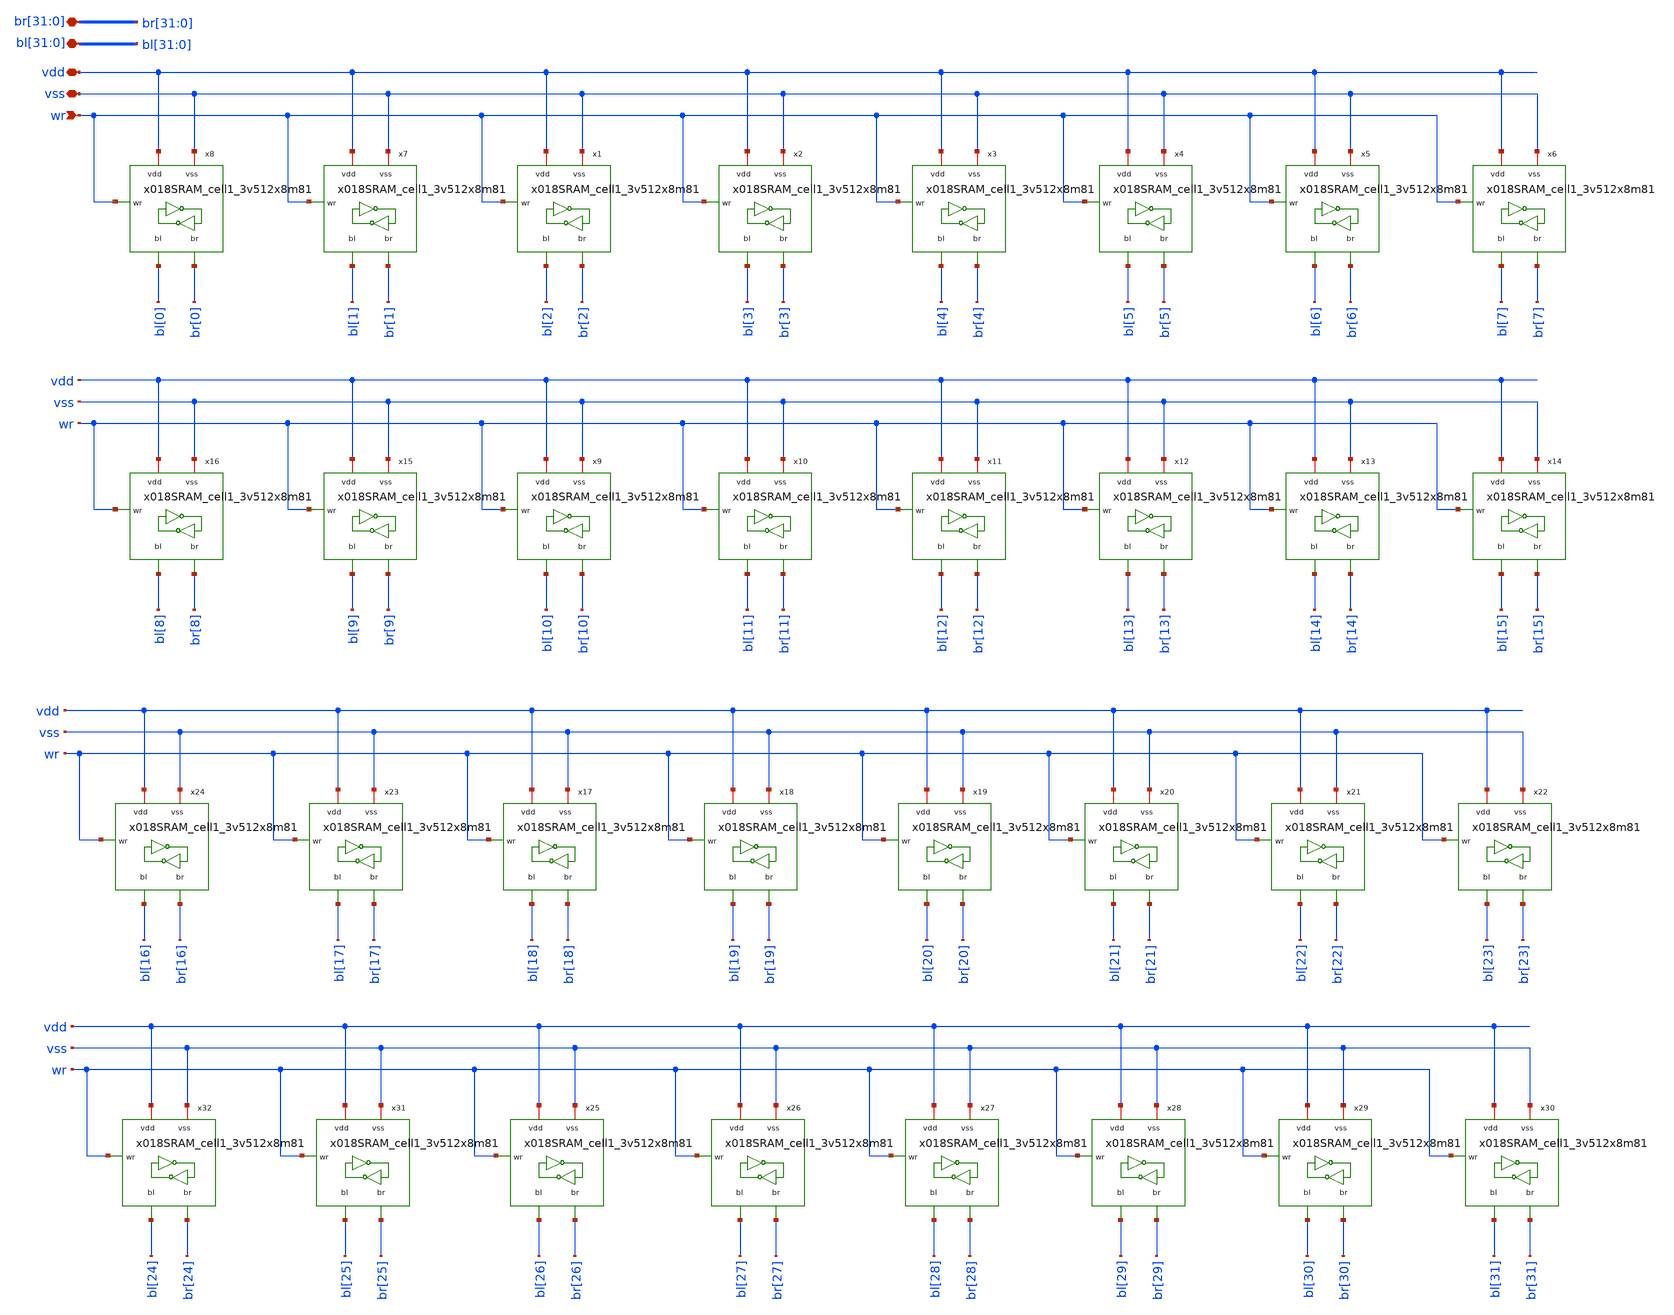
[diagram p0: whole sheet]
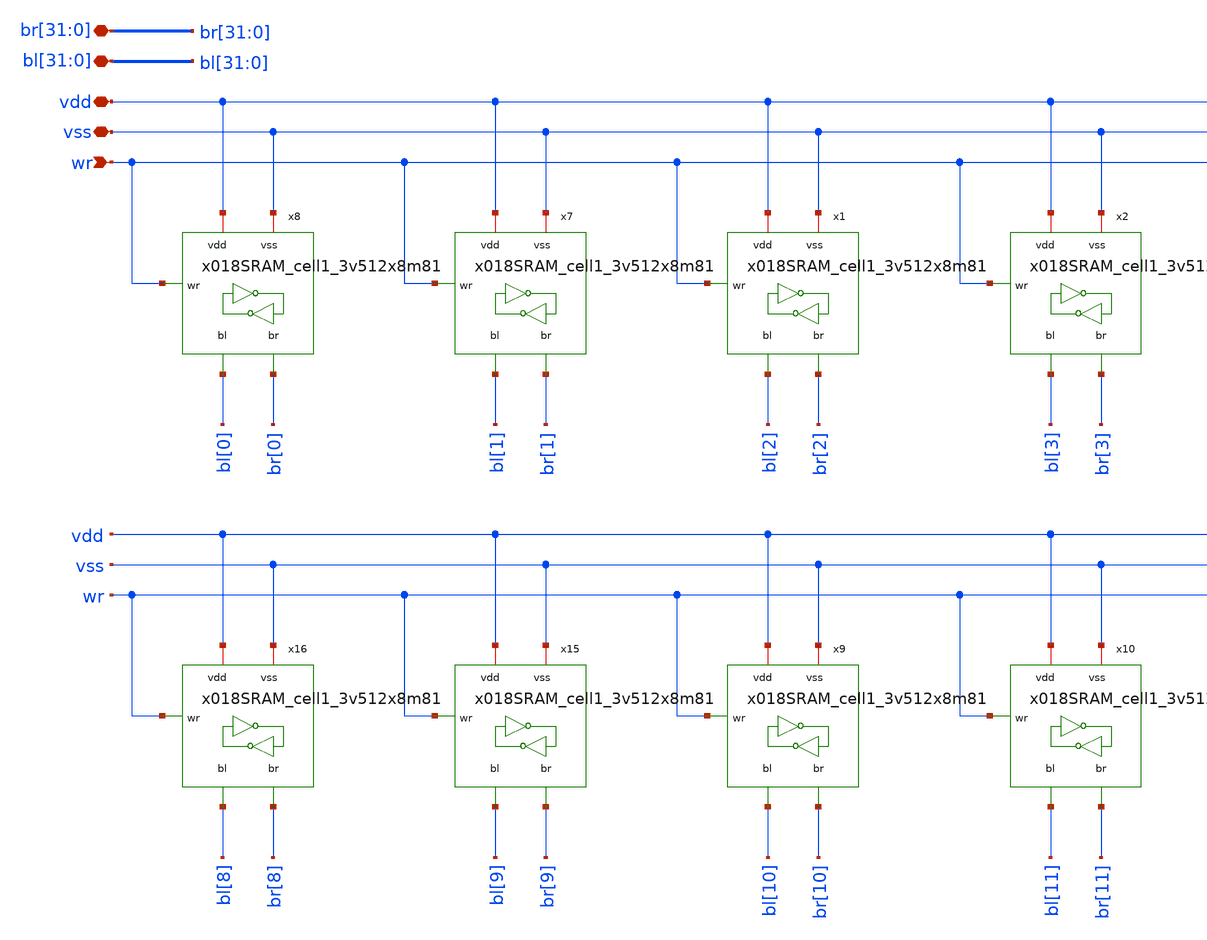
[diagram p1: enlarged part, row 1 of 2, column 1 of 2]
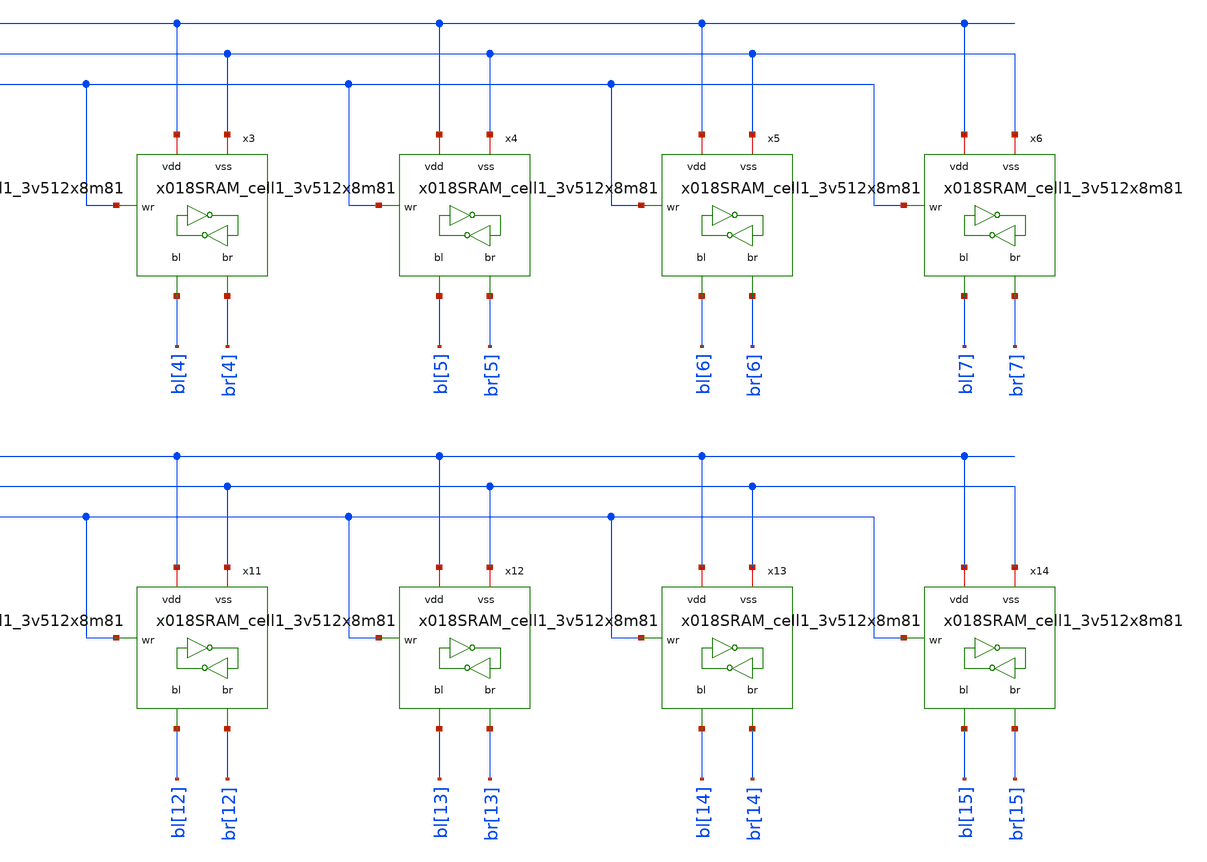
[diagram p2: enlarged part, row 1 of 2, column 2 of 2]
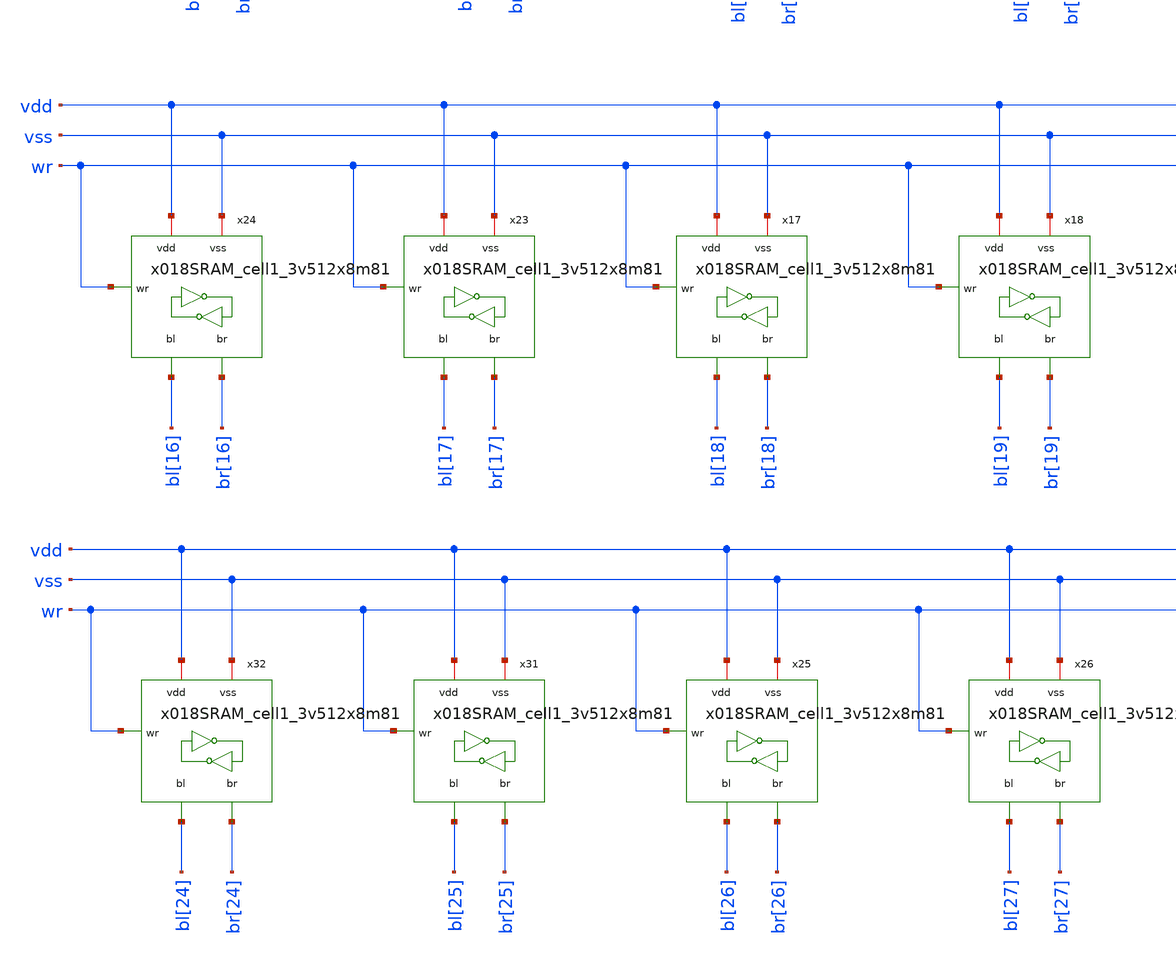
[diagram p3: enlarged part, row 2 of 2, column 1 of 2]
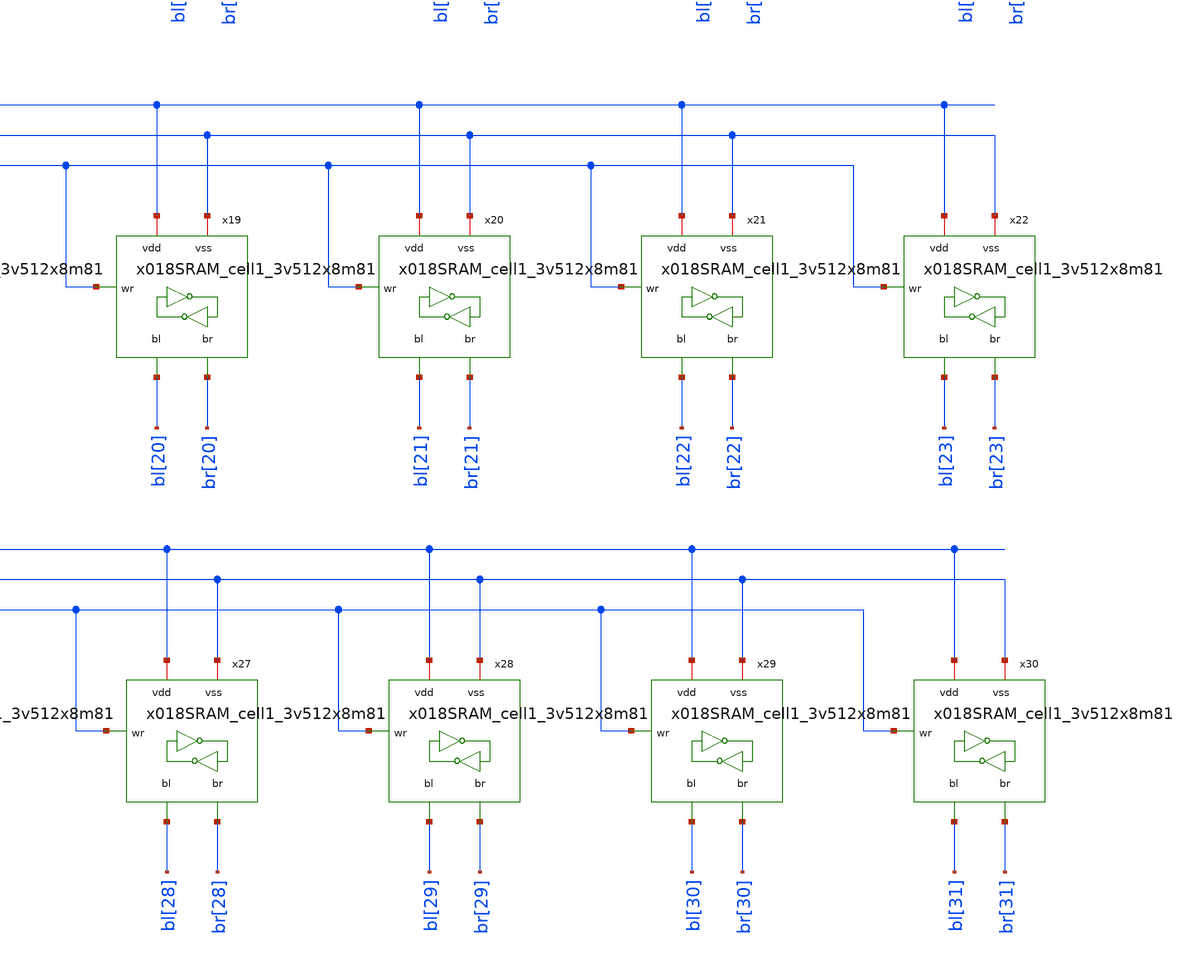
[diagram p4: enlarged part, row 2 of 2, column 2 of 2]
** sch_path: cells/gf180mcu_ocd_ip_sram__sram512x8m8wm1/xschem/Cell_array32x1_3v512x8m81.sch
**.subckt Cell_array32x1_3v512x8m81 vdd vss wr
*+ bl[31],bl[30],bl[29],bl[28],bl[27],bl[26],bl[25],bl[24],bl[23],bl[22],bl[21],bl[20],bl[19],bl[18],bl[17],bl[16],bl[15],bl[14],bl[13],bl[12],bl[11],bl[10],bl[9],bl[8],bl[7],bl[6],bl[5],bl[4],bl[3],bl[2],bl[1],bl[0]
*+ br[31],br[30],br[29],br[28],br[27],br[26],br[25],br[24],br[23],br[22],br[21],br[20],br[19],br[18],br[17],br[16],br[15],br[14],br[13],br[12],br[11],br[10],br[9],br[8],br[7],br[6],br[5],br[4],br[3],br[2],br[1],br[0]
*.iopin vdd
*.iopin vss
*.ipin wr
*.iopin
*+ bl[31],bl[30],bl[29],bl[28],bl[27],bl[26],bl[25],bl[24],bl[23],bl[22],bl[21],bl[20],bl[19],bl[18],bl[17],bl[16],bl[15],bl[14],bl[13],bl[12],bl[11],bl[10],bl[9],bl[8],bl[7],bl[6],bl[5],bl[4],bl[3],bl[2],bl[1],bl[0]
*.iopin
*+ br[31],br[30],br[29],br[28],br[27],br[26],br[25],br[24],br[23],br[22],br[21],br[20],br[19],br[18],br[17],br[16],br[15],br[14],br[13],br[12],br[11],br[10],br[9],br[8],br[7],br[6],br[5],br[4],br[3],br[2],br[1],br[0]
x1 vdd wr bl[2] br[2] vss x018SRAM_cell1_3v512x8m81
x2 vdd wr bl[3] br[3] vss x018SRAM_cell1_3v512x8m81
x3 vdd wr bl[4] br[4] vss x018SRAM_cell1_3v512x8m81
x4 vdd wr bl[5] br[5] vss x018SRAM_cell1_3v512x8m81
x5 vdd wr bl[6] br[6] vss x018SRAM_cell1_3v512x8m81
x6 vdd wr bl[7] br[7] vss x018SRAM_cell1_3v512x8m81
x7 vdd wr bl[1] br[1] vss x018SRAM_cell1_3v512x8m81
x8 vdd wr bl[0] br[0] vss x018SRAM_cell1_3v512x8m81
x9 vdd wr bl[10] br[10] vss x018SRAM_cell1_3v512x8m81
x10 vdd wr bl[11] br[11] vss x018SRAM_cell1_3v512x8m81
x11 vdd wr bl[12] br[12] vss x018SRAM_cell1_3v512x8m81
x12 vdd wr bl[13] br[13] vss x018SRAM_cell1_3v512x8m81
x13 vdd wr bl[14] br[14] vss x018SRAM_cell1_3v512x8m81
x14 vdd wr bl[15] br[15] vss x018SRAM_cell1_3v512x8m81
x15 vdd wr bl[9] br[9] vss x018SRAM_cell1_3v512x8m81
x16 vdd wr bl[8] br[8] vss x018SRAM_cell1_3v512x8m81
x17 vdd wr bl[18] br[18] vss x018SRAM_cell1_3v512x8m81
x18 vdd wr bl[19] br[19] vss x018SRAM_cell1_3v512x8m81
x19 vdd wr bl[20] br[20] vss x018SRAM_cell1_3v512x8m81
x20 vdd wr bl[21] br[21] vss x018SRAM_cell1_3v512x8m81
x21 vdd wr bl[22] br[22] vss x018SRAM_cell1_3v512x8m81
x22 vdd wr bl[23] br[23] vss x018SRAM_cell1_3v512x8m81
x23 vdd wr bl[17] br[17] vss x018SRAM_cell1_3v512x8m81
x24 vdd wr bl[16] br[16] vss x018SRAM_cell1_3v512x8m81
x25 vdd wr bl[26] br[26] vss x018SRAM_cell1_3v512x8m81
x26 vdd wr bl[27] br[27] vss x018SRAM_cell1_3v512x8m81
x27 vdd wr bl[28] br[28] vss x018SRAM_cell1_3v512x8m81
x28 vdd wr bl[29] br[29] vss x018SRAM_cell1_3v512x8m81
x29 vdd wr bl[30] br[30] vss x018SRAM_cell1_3v512x8m81
x30 vdd wr bl[31] br[31] vss x018SRAM_cell1_3v512x8m81
x31 vdd wr bl[25] br[25] vss x018SRAM_cell1_3v512x8m81
x32 vdd wr bl[24] br[24] vss x018SRAM_cell1_3v512x8m81
**.ends
.end
